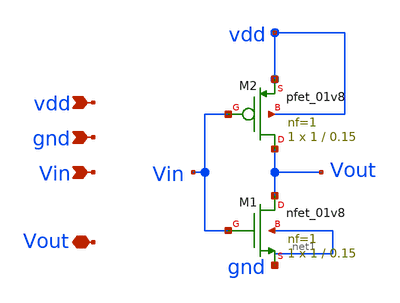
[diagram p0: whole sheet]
** sch_path: ringosci/inverter.sch
**.subckt inverter vdd gnd Vin Vout
*.ipin vdd
*.ipin gnd
*.ipin Vin
*.iopin Vout
XM1 Vout Vin gnd net1 sky130_fd_pr__nfet_01v8 L=0.15 W=1 nf=1 ad='int((nf+1)/2) * W/nf * 0.29' as='int((nf+2)/2) * W/nf * 0.29'
+ pd='2*int((nf+1)/2) * (W/nf + 0.29)' ps='2*int((nf+2)/2) * (W/nf + 0.29)' nrd='0.29 / W' nrs='0.29 / W'
+ sa=0 sb=0 sd=0 mult=1 m=1
XM2 Vout Vin vdd vdd sky130_fd_pr__pfet_01v8 L=0.15 W=1 nf=1 ad='int((nf+1)/2) * W/nf * 0.29' as='int((nf+2)/2) * W/nf * 0.29'
+ pd='2*int((nf+1)/2) * (W/nf + 0.29)' ps='2*int((nf+2)/2) * (W/nf + 0.29)' nrd='0.29 / W' nrs='0.29 / W'
+ sa=0 sb=0 sd=0 mult=1 m=1
**.ends
.end
